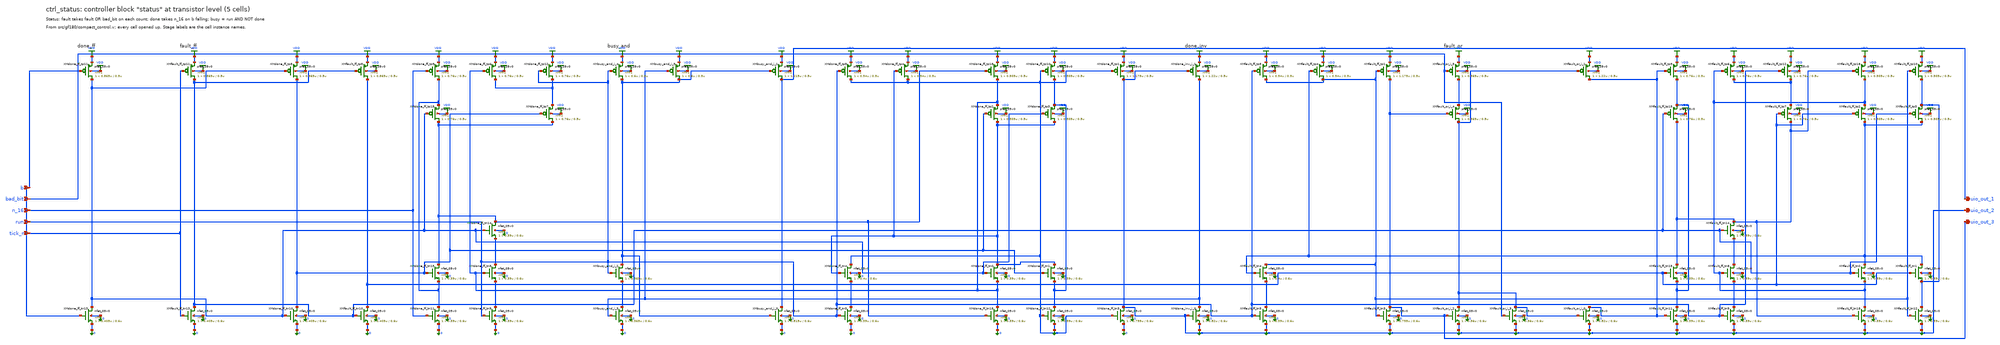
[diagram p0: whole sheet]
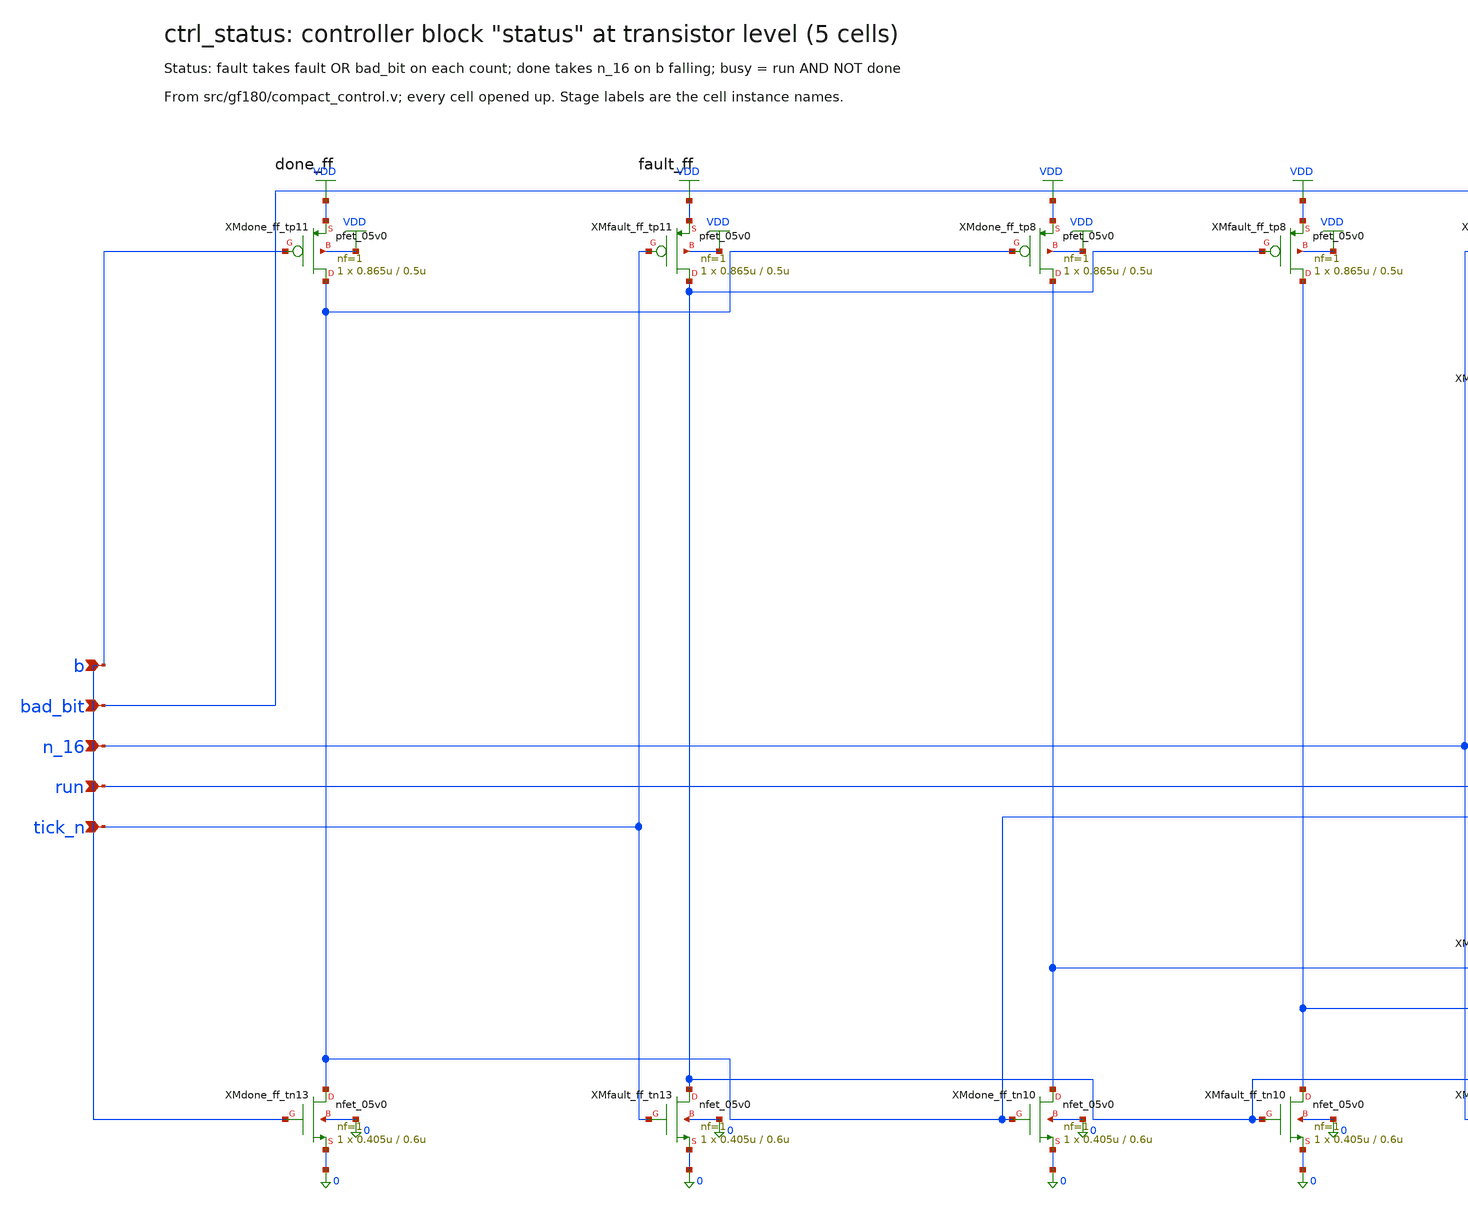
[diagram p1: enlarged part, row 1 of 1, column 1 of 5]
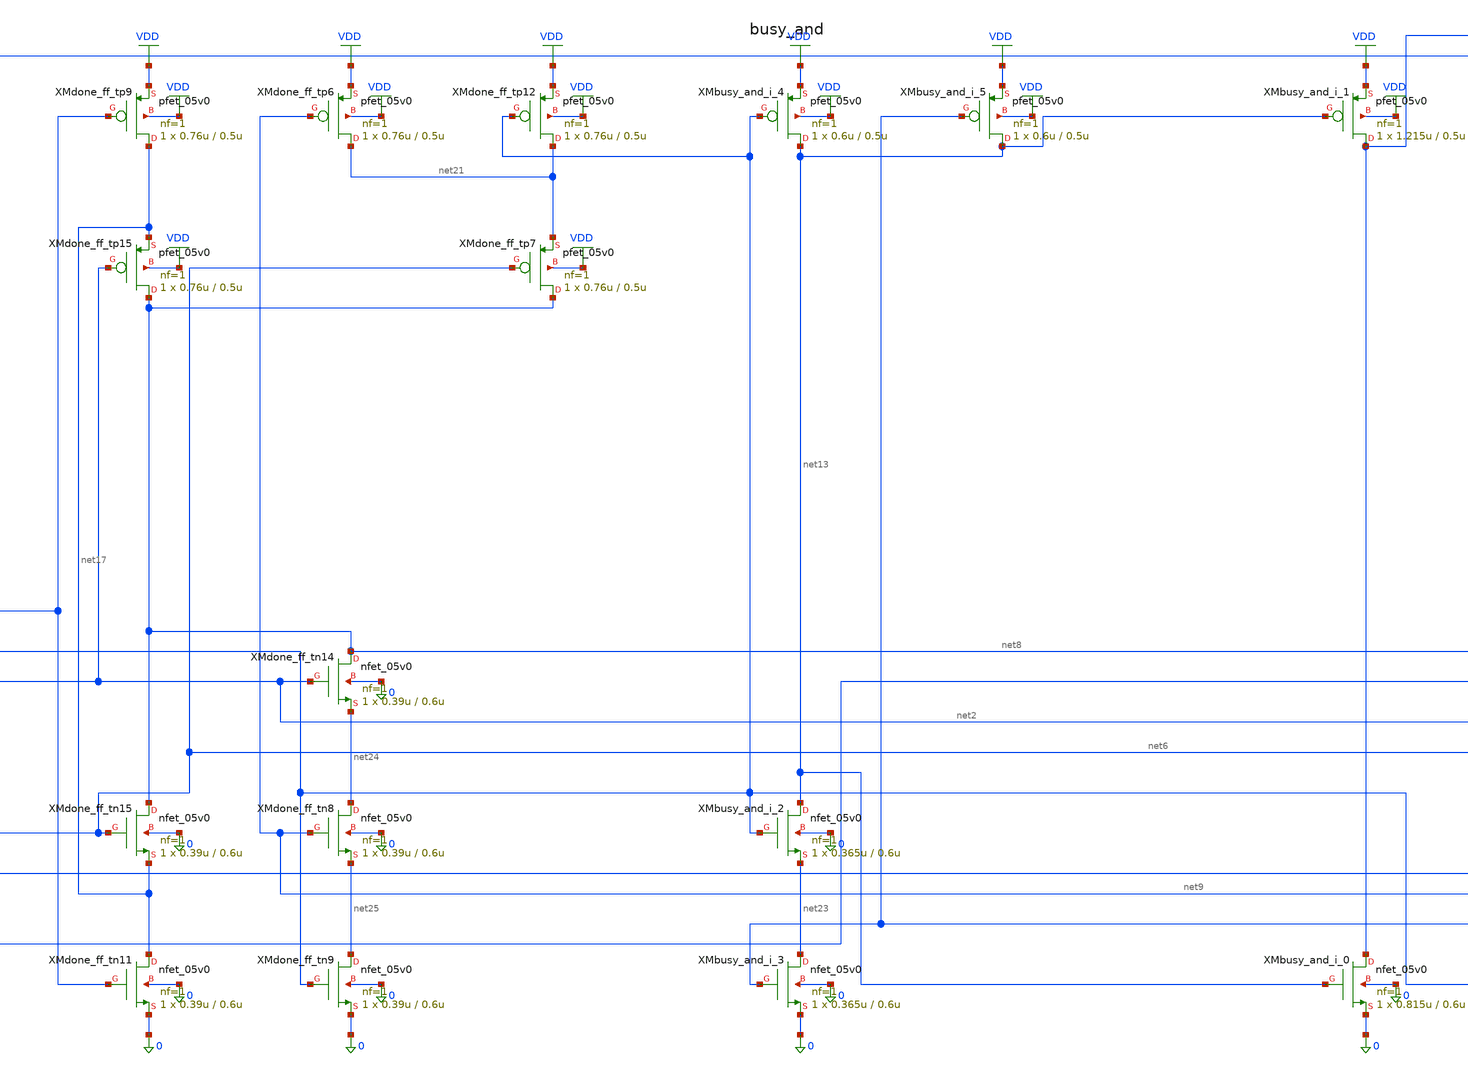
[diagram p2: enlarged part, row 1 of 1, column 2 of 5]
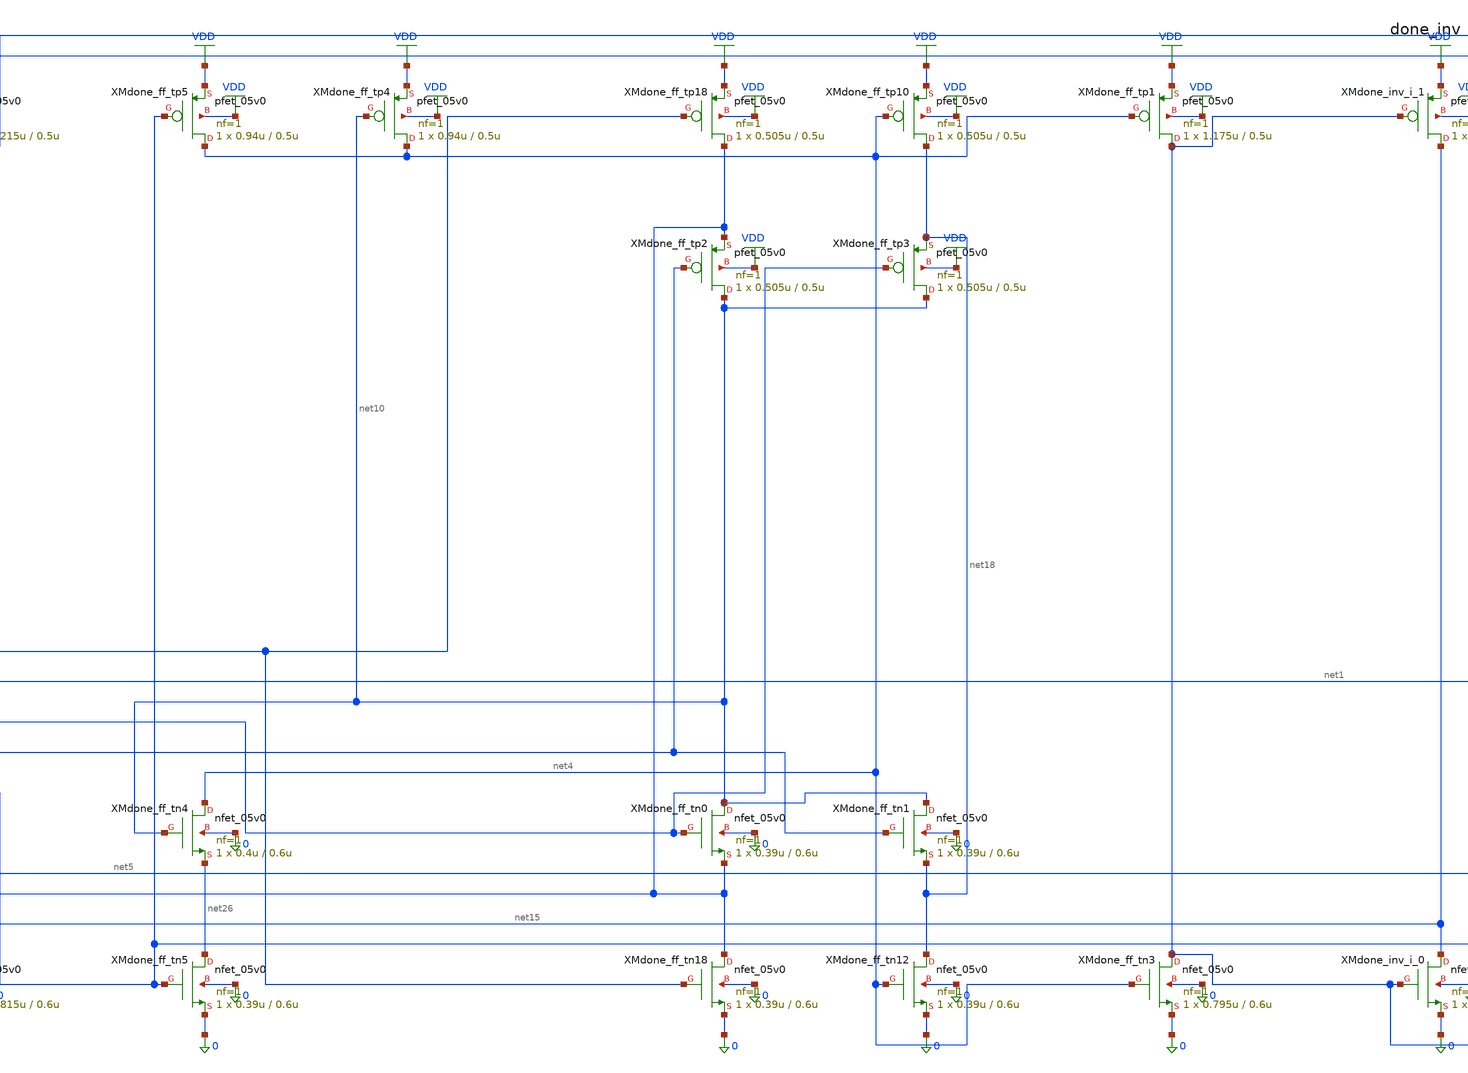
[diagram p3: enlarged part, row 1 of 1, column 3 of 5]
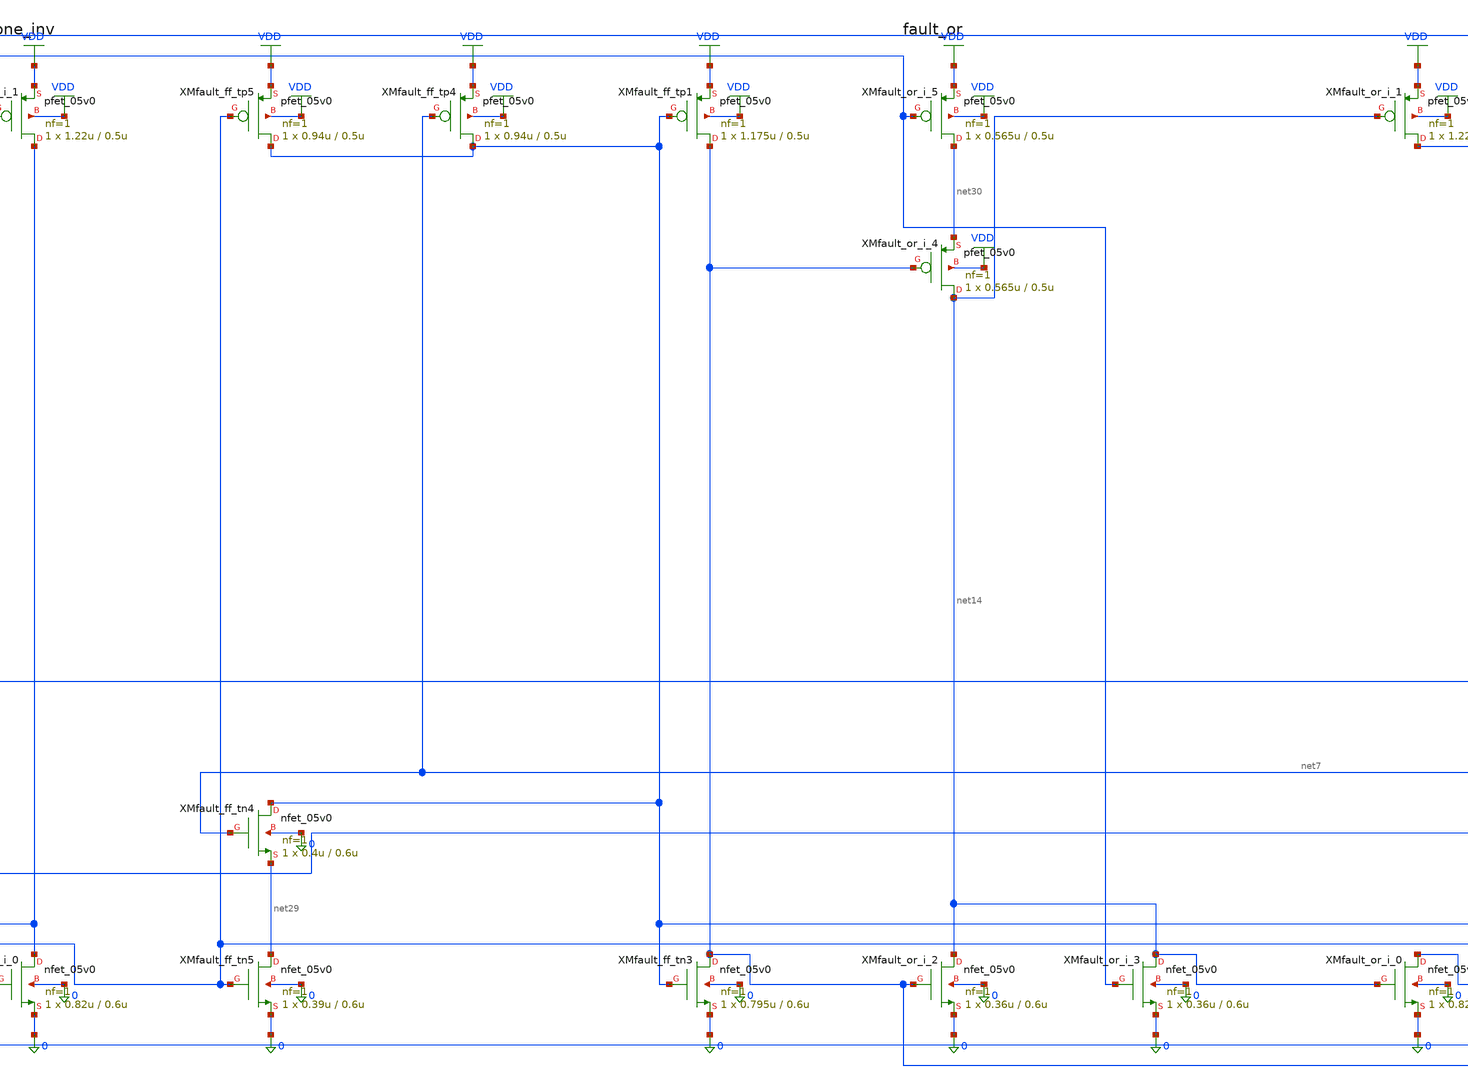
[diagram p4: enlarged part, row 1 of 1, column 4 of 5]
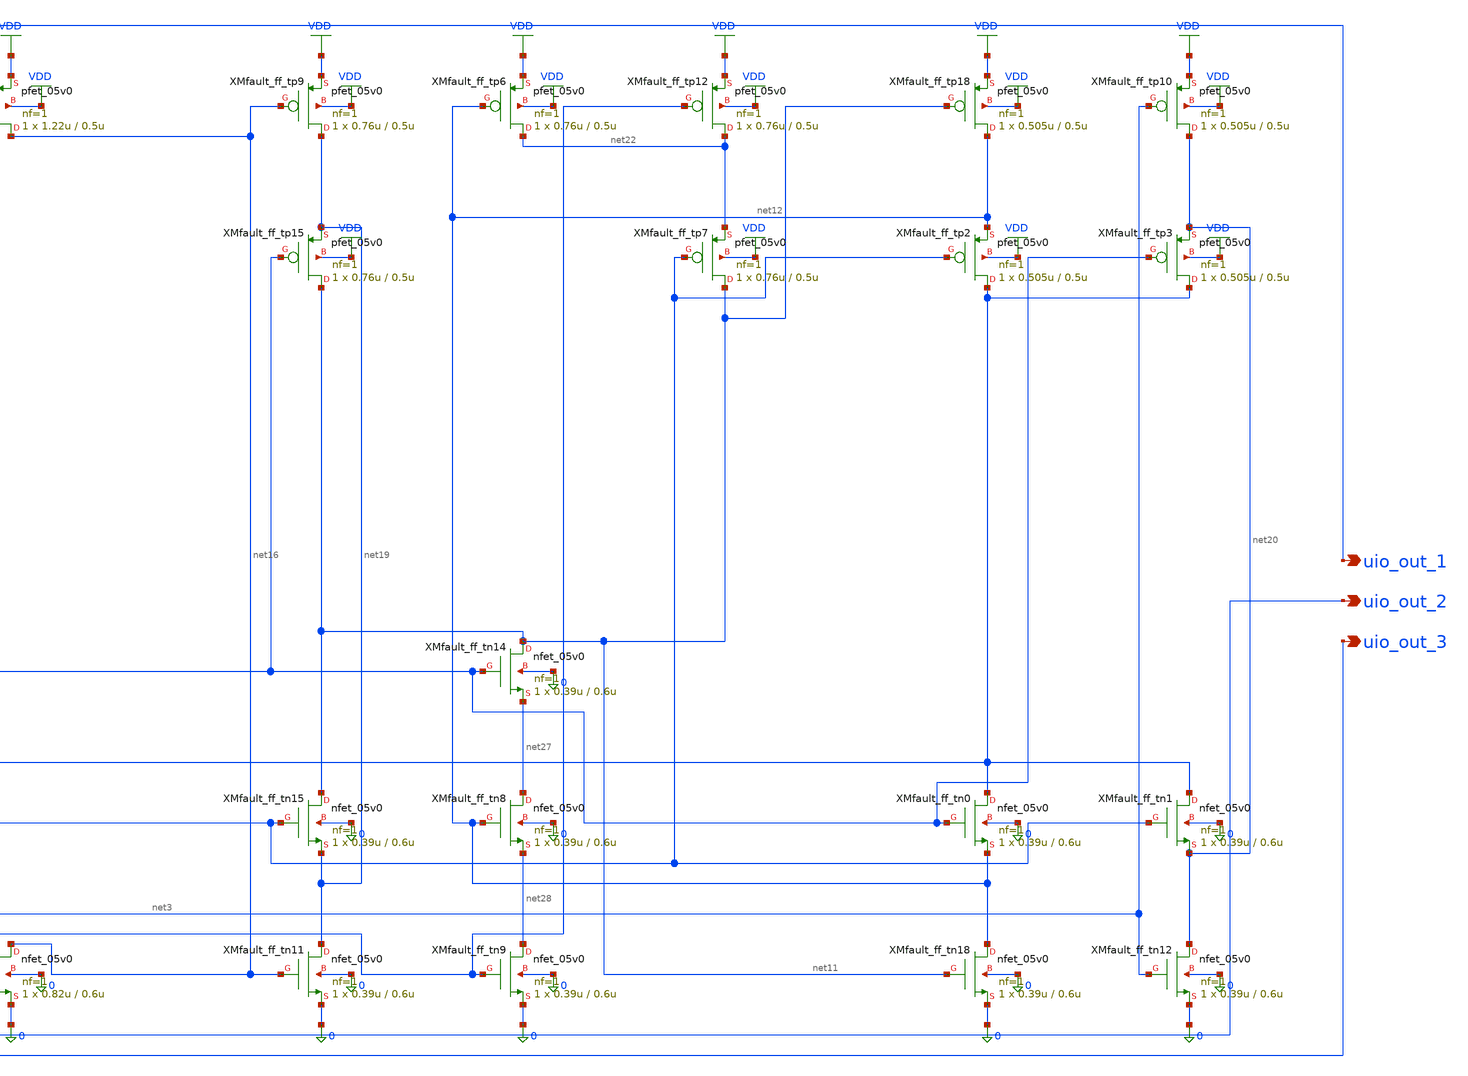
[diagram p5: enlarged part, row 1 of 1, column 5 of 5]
** sch_path: xschem/flat/ctrl_status.sch
**.subckt ctrl_status b bad_bit n_16 run tick_n uio_out_1 uio_out_2 uio_out_3
*.ipin b
*.ipin bad_bit
*.ipin n_16
*.ipin run
*.ipin tick_n
*.opin uio_out_1
*.opin uio_out_2
*.opin uio_out_3
XMbusy_and_i_2 net13 run net23 0 nfet_05v0 L=0.6u W=0.365u nf=1 ad=1.825e-13 as=1.825e-13
+ pd=1.73e-06 ps=1.73e-06 nrd=0 nrs=0 sa=0 sb=0 sd=0 m=1
XMbusy_and_i_3 net23 net15 0 0 nfet_05v0 L=0.6u W=0.365u nf=1 ad=1.825e-13 as=1.825e-13 pd=1.73e-06
+ ps=1.73e-06 nrd=0 nrs=0 sa=0 sb=0 sd=0 m=1
XMbusy_and_i_0 uio_out_1 net13 0 0 nfet_05v0 L=0.6u W=0.815u nf=1 ad=4.075e-13 as=4.075e-13
+ pd=2.63e-06 ps=2.63e-06 nrd=0 nrs=0 sa=0 sb=0 sd=0 m=1
XMbusy_and_i_4 net13 run VDD VDD pfet_05v0 L=0.5u W=0.6u nf=1 ad=3e-13 as=3e-13 pd=2.2e-06
+ ps=2.2e-06 nrd=0 nrs=0 sa=0 sb=0 sd=0 m=1
XMbusy_and_i_5 net13 net15 VDD VDD pfet_05v0 L=0.5u W=0.6u nf=1 ad=3e-13 as=3e-13 pd=2.2e-06
+ ps=2.2e-06 nrd=0 nrs=0 sa=0 sb=0 sd=0 m=1
XMbusy_and_i_1 uio_out_1 net13 VDD VDD pfet_05v0 L=0.5u W=1.215u nf=1 ad=6.075e-13 as=6.075e-13
+ pd=3.43e-06 ps=3.43e-06 nrd=0 nrs=0 sa=0 sb=0 sd=0 m=1
XMdone_ff_tn13 net2 b 0 0 nfet_05v0 L=0.6u W=0.405u nf=1 ad=2.025e-13 as=2.025e-13 pd=1.81e-06
+ ps=1.81e-06 nrd=0 nrs=0 sa=0 sb=0 sd=0 m=1
XMdone_ff_tn10 net6 net2 0 0 nfet_05v0 L=0.6u W=0.405u nf=1 ad=2.025e-13 as=2.025e-13 pd=1.81e-06
+ ps=1.81e-06 nrd=0 nrs=0 sa=0 sb=0 sd=0 m=1
XMdone_ff_tn11 net17 n_16 0 0 nfet_05v0 L=0.6u W=0.39u nf=1 ad=1.95e-13 as=1.95e-13 pd=1.78e-06
+ ps=1.78e-06 nrd=0 nrs=0 sa=0 sb=0 sd=0 m=1
XMdone_ff_tn15 net8 net6 net17 0 nfet_05v0 L=0.6u W=0.39u nf=1 ad=1.95e-13 as=1.95e-13 pd=1.78e-06
+ ps=1.78e-06 nrd=0 nrs=0 sa=0 sb=0 sd=0 m=1
XMdone_ff_tn14 net8 net2 net24 0 nfet_05v0 L=0.6u W=0.39u nf=1 ad=1.95e-13 as=1.95e-13 pd=1.78e-06
+ ps=1.78e-06 nrd=0 nrs=0 sa=0 sb=0 sd=0 m=1
XMdone_ff_tn8 net24 net9 net25 0 nfet_05v0 L=0.6u W=0.39u nf=1 ad=1.95e-13 as=1.95e-13 pd=1.78e-06
+ ps=1.78e-06 nrd=0 nrs=0 sa=0 sb=0 sd=0 m=1
XMdone_ff_tn9 net25 run 0 0 nfet_05v0 L=0.6u W=0.39u nf=1 ad=1.95e-13 as=1.95e-13 pd=1.78e-06
+ ps=1.78e-06 nrd=0 nrs=0 sa=0 sb=0 sd=0 m=1
XMdone_ff_tn18 net9 net8 0 0 nfet_05v0 L=0.6u W=0.39u nf=1 ad=1.95e-13 as=1.95e-13 pd=1.78e-06
+ ps=1.78e-06 nrd=0 nrs=0 sa=0 sb=0 sd=0 m=1
XMdone_ff_tn0 net10 net2 net9 0 nfet_05v0 L=0.6u W=0.39u nf=1 ad=1.95e-13 as=1.95e-13 pd=1.78e-06
+ ps=1.78e-06 nrd=0 nrs=0 sa=0 sb=0 sd=0 m=1
XMdone_ff_tn1 net10 net6 net18 0 nfet_05v0 L=0.6u W=0.39u nf=1 ad=1.95e-13 as=1.95e-13 pd=1.78e-06
+ ps=1.78e-06 nrd=0 nrs=0 sa=0 sb=0 sd=0 m=1
XMdone_ff_tn12 net18 net4 0 0 nfet_05v0 L=0.6u W=0.39u nf=1 ad=1.95e-13 as=1.95e-13 pd=1.78e-06
+ ps=1.78e-06 nrd=0 nrs=0 sa=0 sb=0 sd=0 m=1
XMdone_ff_tn5 net26 run 0 0 nfet_05v0 L=0.6u W=0.39u nf=1 ad=1.95e-13 as=1.95e-13 pd=1.78e-06
+ ps=1.78e-06 nrd=0 nrs=0 sa=0 sb=0 sd=0 m=1
XMdone_ff_tn4 net4 net10 net26 0 nfet_05v0 L=0.6u W=0.4u nf=1 ad=2e-13 as=2e-13 pd=1.8e-06
+ ps=1.8e-06 nrd=0 nrs=0 sa=0 sb=0 sd=0 m=1
XMdone_ff_tn3 uio_out_2 net4 0 0 nfet_05v0 L=0.6u W=0.795u nf=1 ad=3.975e-13 as=3.975e-13
+ pd=2.59e-06 ps=2.59e-06 nrd=0 nrs=0 sa=0 sb=0 sd=0 m=1
XMdone_ff_tp11 net2 b VDD VDD pfet_05v0 L=0.5u W=0.865u nf=1 ad=4.325e-13 as=4.325e-13 pd=2.73e-06
+ ps=2.73e-06 nrd=0 nrs=0 sa=0 sb=0 sd=0 m=1
XMdone_ff_tp8 net6 net2 VDD VDD pfet_05v0 L=0.5u W=0.865u nf=1 ad=4.325e-13 as=4.325e-13 pd=2.73e-06
+ ps=2.73e-06 nrd=0 nrs=0 sa=0 sb=0 sd=0 m=1
XMdone_ff_tp9 net17 n_16 VDD VDD pfet_05v0 L=0.5u W=0.76u nf=1 ad=3.8e-13 as=3.8e-13 pd=2.52e-06
+ ps=2.52e-06 nrd=0 nrs=0 sa=0 sb=0 sd=0 m=1
XMdone_ff_tp15 net8 net2 net17 VDD pfet_05v0 L=0.5u W=0.76u nf=1 ad=3.8e-13 as=3.8e-13 pd=2.52e-06
+ ps=2.52e-06 nrd=0 nrs=0 sa=0 sb=0 sd=0 m=1
XMdone_ff_tp7 net8 net6 net21 VDD pfet_05v0 L=0.5u W=0.76u nf=1 ad=3.8e-13 as=3.8e-13 pd=2.52e-06
+ ps=2.52e-06 nrd=0 nrs=0 sa=0 sb=0 sd=0 m=1
XMdone_ff_tp6 net21 net9 VDD VDD pfet_05v0 L=0.5u W=0.76u nf=1 ad=3.8e-13 as=3.8e-13 pd=2.52e-06
+ ps=2.52e-06 nrd=0 nrs=0 sa=0 sb=0 sd=0 m=1
XMdone_ff_tp12 net21 run VDD VDD pfet_05v0 L=0.5u W=0.76u nf=1 ad=3.8e-13 as=3.8e-13 pd=2.52e-06
+ ps=2.52e-06 nrd=0 nrs=0 sa=0 sb=0 sd=0 m=1
XMdone_ff_tp18 net9 net8 VDD VDD pfet_05v0 L=0.5u W=0.505u nf=1 ad=2.525e-13 as=2.525e-13
+ pd=2.01e-06 ps=2.01e-06 nrd=0 nrs=0 sa=0 sb=0 sd=0 m=1
XMdone_ff_tp2 net10 net6 net9 VDD pfet_05v0 L=0.5u W=0.505u nf=1 ad=2.525e-13 as=2.525e-13
+ pd=2.01e-06 ps=2.01e-06 nrd=0 nrs=0 sa=0 sb=0 sd=0 m=1
XMdone_ff_tp3 net10 net2 net18 VDD pfet_05v0 L=0.5u W=0.505u nf=1 ad=2.525e-13 as=2.525e-13
+ pd=2.01e-06 ps=2.01e-06 nrd=0 nrs=0 sa=0 sb=0 sd=0 m=1
XMdone_ff_tp10 net18 net4 VDD VDD pfet_05v0 L=0.5u W=0.505u nf=1 ad=2.525e-13 as=2.525e-13
+ pd=2.01e-06 ps=2.01e-06 nrd=0 nrs=0 sa=0 sb=0 sd=0 m=1
XMdone_ff_tp5 net4 run VDD VDD pfet_05v0 L=0.5u W=0.94u nf=1 ad=4.7e-13 as=4.7e-13 pd=2.88e-06
+ ps=2.88e-06 nrd=0 nrs=0 sa=0 sb=0 sd=0 m=1
XMdone_ff_tp4 net4 net10 VDD VDD pfet_05v0 L=0.5u W=0.94u nf=1 ad=4.7e-13 as=4.7e-13 pd=2.88e-06
+ ps=2.88e-06 nrd=0 nrs=0 sa=0 sb=0 sd=0 m=1
XMdone_ff_tp1 uio_out_2 net4 VDD VDD pfet_05v0 L=0.5u W=1.175u nf=1 ad=5.875e-13 as=5.875e-13
+ pd=3.35e-06 ps=3.35e-06 nrd=0 nrs=0 sa=0 sb=0 sd=0 m=1
XMdone_inv_i_0 net15 uio_out_2 0 0 nfet_05v0 L=0.6u W=0.82u nf=1 ad=4.1e-13 as=4.1e-13 pd=2.64e-06
+ ps=2.64e-06 nrd=0 nrs=0 sa=0 sb=0 sd=0 m=1
XMdone_inv_i_1 net15 uio_out_2 VDD VDD pfet_05v0 L=0.5u W=1.22u nf=1 ad=6.1e-13 as=6.1e-13
+ pd=3.44e-06 ps=3.44e-06 nrd=0 nrs=0 sa=0 sb=0 sd=0 m=1
XMfault_ff_tn13 net1 tick_n 0 0 nfet_05v0 L=0.6u W=0.405u nf=1 ad=2.025e-13 as=2.025e-13 pd=1.81e-06
+ ps=1.81e-06 nrd=0 nrs=0 sa=0 sb=0 sd=0 m=1
XMfault_ff_tn10 net5 net1 0 0 nfet_05v0 L=0.6u W=0.405u nf=1 ad=2.025e-13 as=2.025e-13 pd=1.81e-06
+ ps=1.81e-06 nrd=0 nrs=0 sa=0 sb=0 sd=0 m=1
XMfault_ff_tn11 net19 net16 0 0 nfet_05v0 L=0.6u W=0.39u nf=1 ad=1.95e-13 as=1.95e-13 pd=1.78e-06
+ ps=1.78e-06 nrd=0 nrs=0 sa=0 sb=0 sd=0 m=1
XMfault_ff_tn15 net11 net5 net19 0 nfet_05v0 L=0.6u W=0.39u nf=1 ad=1.95e-13 as=1.95e-13 pd=1.78e-06
+ ps=1.78e-06 nrd=0 nrs=0 sa=0 sb=0 sd=0 m=1
XMfault_ff_tn14 net11 net1 net27 0 nfet_05v0 L=0.6u W=0.39u nf=1 ad=1.95e-13 as=1.95e-13 pd=1.78e-06
+ ps=1.78e-06 nrd=0 nrs=0 sa=0 sb=0 sd=0 m=1
XMfault_ff_tn8 net27 net12 net28 0 nfet_05v0 L=0.6u W=0.39u nf=1 ad=1.95e-13 as=1.95e-13 pd=1.78e-06
+ ps=1.78e-06 nrd=0 nrs=0 sa=0 sb=0 sd=0 m=1
XMfault_ff_tn9 net28 run 0 0 nfet_05v0 L=0.6u W=0.39u nf=1 ad=1.95e-13 as=1.95e-13 pd=1.78e-06
+ ps=1.78e-06 nrd=0 nrs=0 sa=0 sb=0 sd=0 m=1
XMfault_ff_tn18 net12 net11 0 0 nfet_05v0 L=0.6u W=0.39u nf=1 ad=1.95e-13 as=1.95e-13 pd=1.78e-06
+ ps=1.78e-06 nrd=0 nrs=0 sa=0 sb=0 sd=0 m=1
XMfault_ff_tn0 net7 net1 net12 0 nfet_05v0 L=0.6u W=0.39u nf=1 ad=1.95e-13 as=1.95e-13 pd=1.78e-06
+ ps=1.78e-06 nrd=0 nrs=0 sa=0 sb=0 sd=0 m=1
XMfault_ff_tn1 net7 net5 net20 0 nfet_05v0 L=0.6u W=0.39u nf=1 ad=1.95e-13 as=1.95e-13 pd=1.78e-06
+ ps=1.78e-06 nrd=0 nrs=0 sa=0 sb=0 sd=0 m=1
XMfault_ff_tn12 net20 net3 0 0 nfet_05v0 L=0.6u W=0.39u nf=1 ad=1.95e-13 as=1.95e-13 pd=1.78e-06
+ ps=1.78e-06 nrd=0 nrs=0 sa=0 sb=0 sd=0 m=1
XMfault_ff_tn5 net29 run 0 0 nfet_05v0 L=0.6u W=0.39u nf=1 ad=1.95e-13 as=1.95e-13 pd=1.78e-06
+ ps=1.78e-06 nrd=0 nrs=0 sa=0 sb=0 sd=0 m=1
XMfault_ff_tn4 net3 net7 net29 0 nfet_05v0 L=0.6u W=0.4u nf=1 ad=2e-13 as=2e-13 pd=1.8e-06
+ ps=1.8e-06 nrd=0 nrs=0 sa=0 sb=0 sd=0 m=1
XMfault_ff_tn3 uio_out_3 net3 0 0 nfet_05v0 L=0.6u W=0.795u nf=1 ad=3.975e-13 as=3.975e-13
+ pd=2.59e-06 ps=2.59e-06 nrd=0 nrs=0 sa=0 sb=0 sd=0 m=1
XMfault_ff_tp11 net1 tick_n VDD VDD pfet_05v0 L=0.5u W=0.865u nf=1 ad=4.325e-13 as=4.325e-13
+ pd=2.73e-06 ps=2.73e-06 nrd=0 nrs=0 sa=0 sb=0 sd=0 m=1
XMfault_ff_tp8 net5 net1 VDD VDD pfet_05v0 L=0.5u W=0.865u nf=1 ad=4.325e-13 as=4.325e-13
+ pd=2.73e-06 ps=2.73e-06 nrd=0 nrs=0 sa=0 sb=0 sd=0 m=1
XMfault_ff_tp9 net19 net16 VDD VDD pfet_05v0 L=0.5u W=0.76u nf=1 ad=3.8e-13 as=3.8e-13 pd=2.52e-06
+ ps=2.52e-06 nrd=0 nrs=0 sa=0 sb=0 sd=0 m=1
XMfault_ff_tp15 net11 net1 net19 VDD pfet_05v0 L=0.5u W=0.76u nf=1 ad=3.8e-13 as=3.8e-13 pd=2.52e-06
+ ps=2.52e-06 nrd=0 nrs=0 sa=0 sb=0 sd=0 m=1
XMfault_ff_tp7 net11 net5 net22 VDD pfet_05v0 L=0.5u W=0.76u nf=1 ad=3.8e-13 as=3.8e-13 pd=2.52e-06
+ ps=2.52e-06 nrd=0 nrs=0 sa=0 sb=0 sd=0 m=1
XMfault_ff_tp6 net22 net12 VDD VDD pfet_05v0 L=0.5u W=0.76u nf=1 ad=3.8e-13 as=3.8e-13 pd=2.52e-06
+ ps=2.52e-06 nrd=0 nrs=0 sa=0 sb=0 sd=0 m=1
XMfault_ff_tp12 net22 run VDD VDD pfet_05v0 L=0.5u W=0.76u nf=1 ad=3.8e-13 as=3.8e-13 pd=2.52e-06
+ ps=2.52e-06 nrd=0 nrs=0 sa=0 sb=0 sd=0 m=1
XMfault_ff_tp18 net12 net11 VDD VDD pfet_05v0 L=0.5u W=0.505u nf=1 ad=2.525e-13 as=2.525e-13
+ pd=2.01e-06 ps=2.01e-06 nrd=0 nrs=0 sa=0 sb=0 sd=0 m=1
XMfault_ff_tp2 net7 net5 net12 VDD pfet_05v0 L=0.5u W=0.505u nf=1 ad=2.525e-13 as=2.525e-13
+ pd=2.01e-06 ps=2.01e-06 nrd=0 nrs=0 sa=0 sb=0 sd=0 m=1
XMfault_ff_tp3 net7 net1 net20 VDD pfet_05v0 L=0.5u W=0.505u nf=1 ad=2.525e-13 as=2.525e-13
+ pd=2.01e-06 ps=2.01e-06 nrd=0 nrs=0 sa=0 sb=0 sd=0 m=1
XMfault_ff_tp10 net20 net3 VDD VDD pfet_05v0 L=0.5u W=0.505u nf=1 ad=2.525e-13 as=2.525e-13
+ pd=2.01e-06 ps=2.01e-06 nrd=0 nrs=0 sa=0 sb=0 sd=0 m=1
XMfault_ff_tp5 net3 run VDD VDD pfet_05v0 L=0.5u W=0.94u nf=1 ad=4.7e-13 as=4.7e-13 pd=2.88e-06
+ ps=2.88e-06 nrd=0 nrs=0 sa=0 sb=0 sd=0 m=1
XMfault_ff_tp4 net3 net7 VDD VDD pfet_05v0 L=0.5u W=0.94u nf=1 ad=4.7e-13 as=4.7e-13 pd=2.88e-06
+ ps=2.88e-06 nrd=0 nrs=0 sa=0 sb=0 sd=0 m=1
XMfault_ff_tp1 uio_out_3 net3 VDD VDD pfet_05v0 L=0.5u W=1.175u nf=1 ad=5.875e-13 as=5.875e-13
+ pd=3.35e-06 ps=3.35e-06 nrd=0 nrs=0 sa=0 sb=0 sd=0 m=1
XMfault_or_i_2 net14 uio_out_3 0 0 nfet_05v0 L=0.6u W=0.36u nf=1 ad=1.8e-13 as=1.8e-13 pd=1.72e-06
+ ps=1.72e-06 nrd=0 nrs=0 sa=0 sb=0 sd=0 m=1
XMfault_or_i_3 net14 bad_bit 0 0 nfet_05v0 L=0.6u W=0.36u nf=1 ad=1.8e-13 as=1.8e-13 pd=1.72e-06
+ ps=1.72e-06 nrd=0 nrs=0 sa=0 sb=0 sd=0 m=1
XMfault_or_i_0 net16 net14 0 0 nfet_05v0 L=0.6u W=0.82u nf=1 ad=4.1e-13 as=4.1e-13 pd=2.64e-06
+ ps=2.64e-06 nrd=0 nrs=0 sa=0 sb=0 sd=0 m=1
XMfault_or_i_4 net14 uio_out_3 net30 VDD pfet_05v0 L=0.5u W=0.565u nf=1 ad=2.825e-13 as=2.825e-13
+ pd=2.13e-06 ps=2.13e-06 nrd=0 nrs=0 sa=0 sb=0 sd=0 m=1
XMfault_or_i_5 net30 bad_bit VDD VDD pfet_05v0 L=0.5u W=0.565u nf=1 ad=2.825e-13 as=2.825e-13
+ pd=2.13e-06 ps=2.13e-06 nrd=0 nrs=0 sa=0 sb=0 sd=0 m=1
XMfault_or_i_1 net16 net14 VDD VDD pfet_05v0 L=0.5u W=1.22u nf=1 ad=6.1e-13 as=6.1e-13 pd=3.44e-06
+ ps=3.44e-06 nrd=0 nrs=0 sa=0 sb=0 sd=0 m=1
**.ends
.GLOBAL VDD
.end
